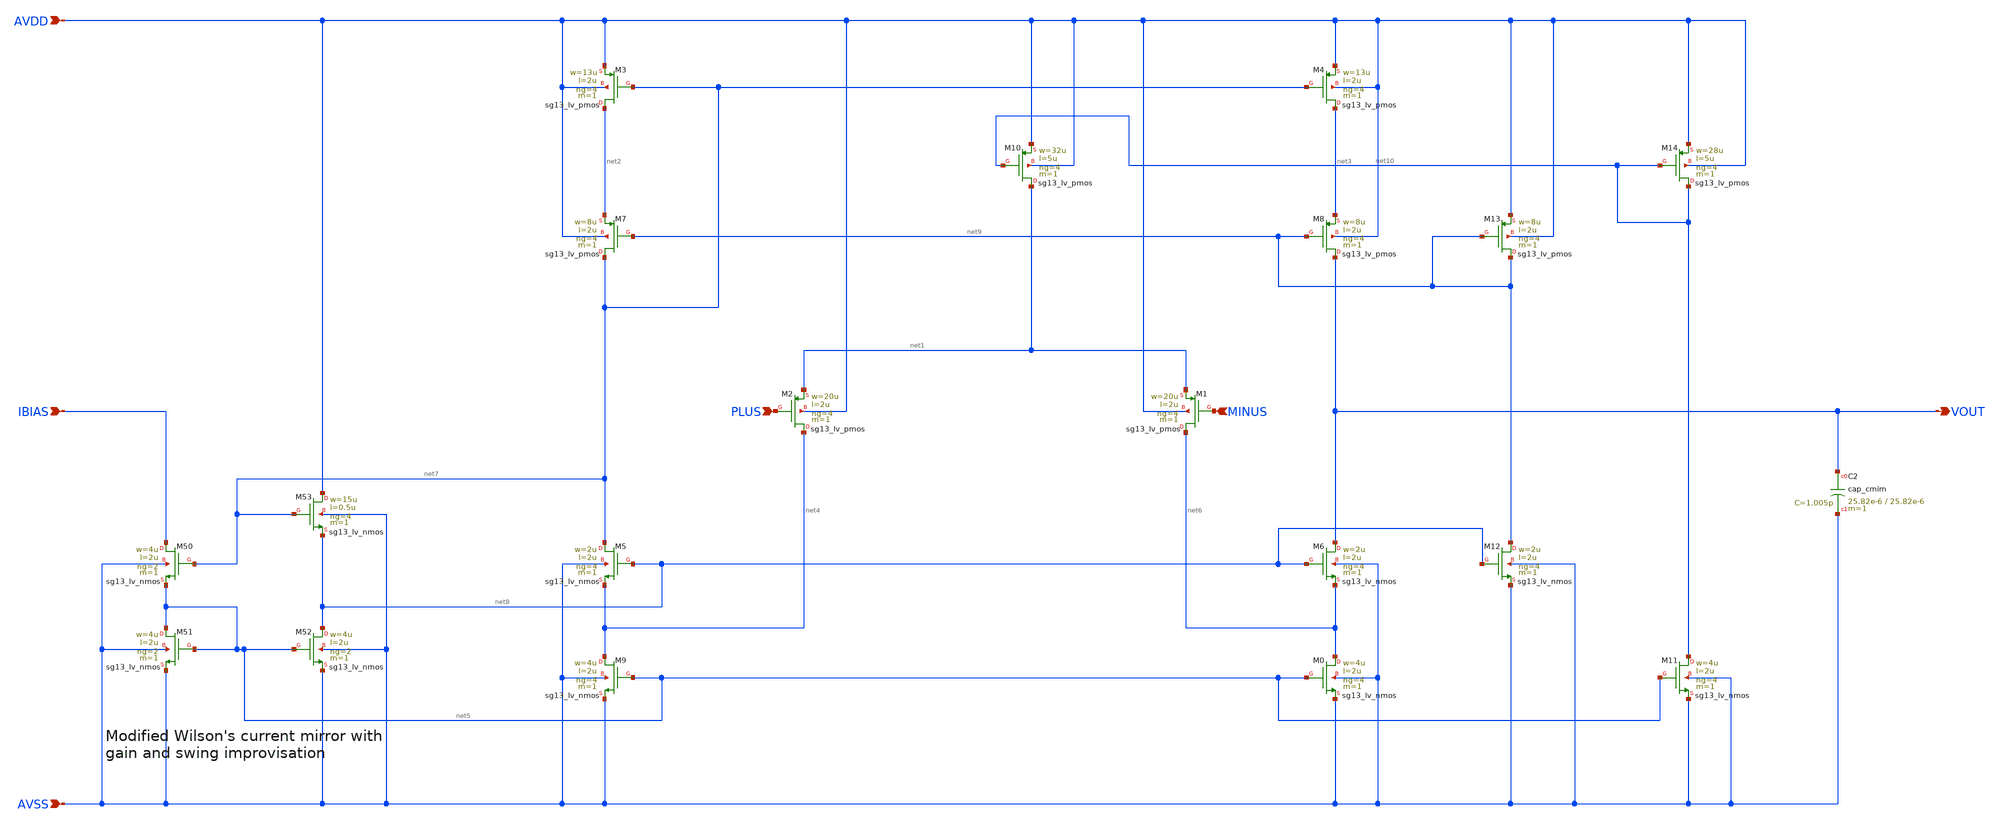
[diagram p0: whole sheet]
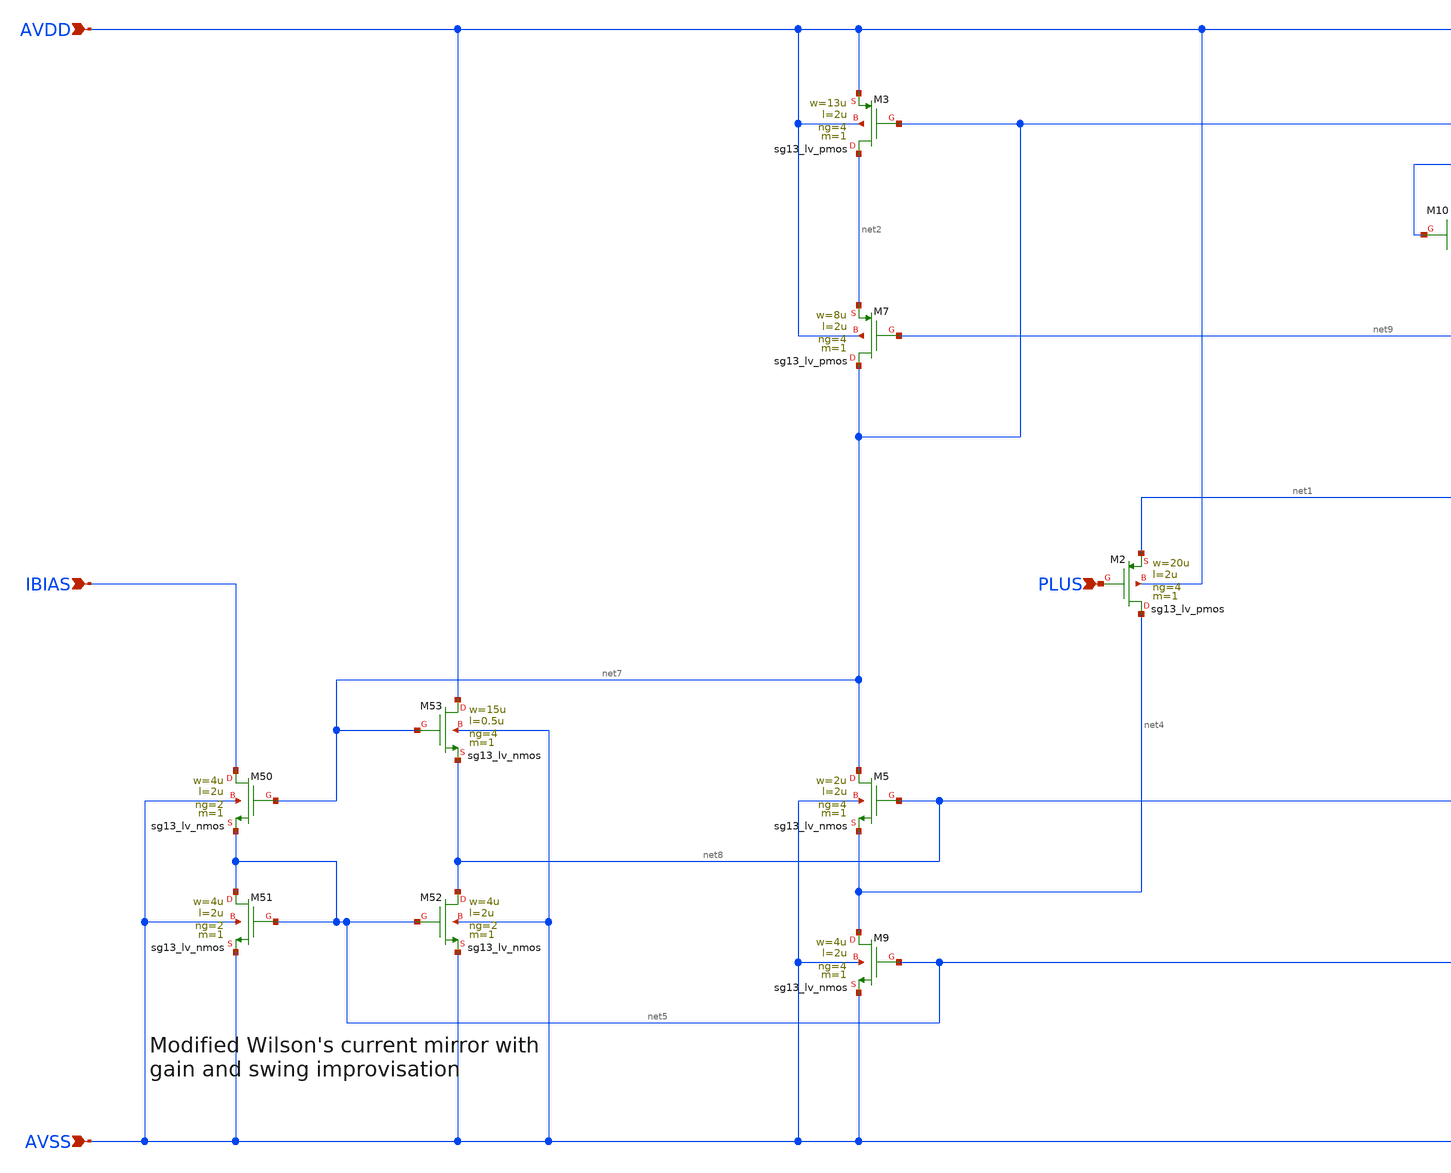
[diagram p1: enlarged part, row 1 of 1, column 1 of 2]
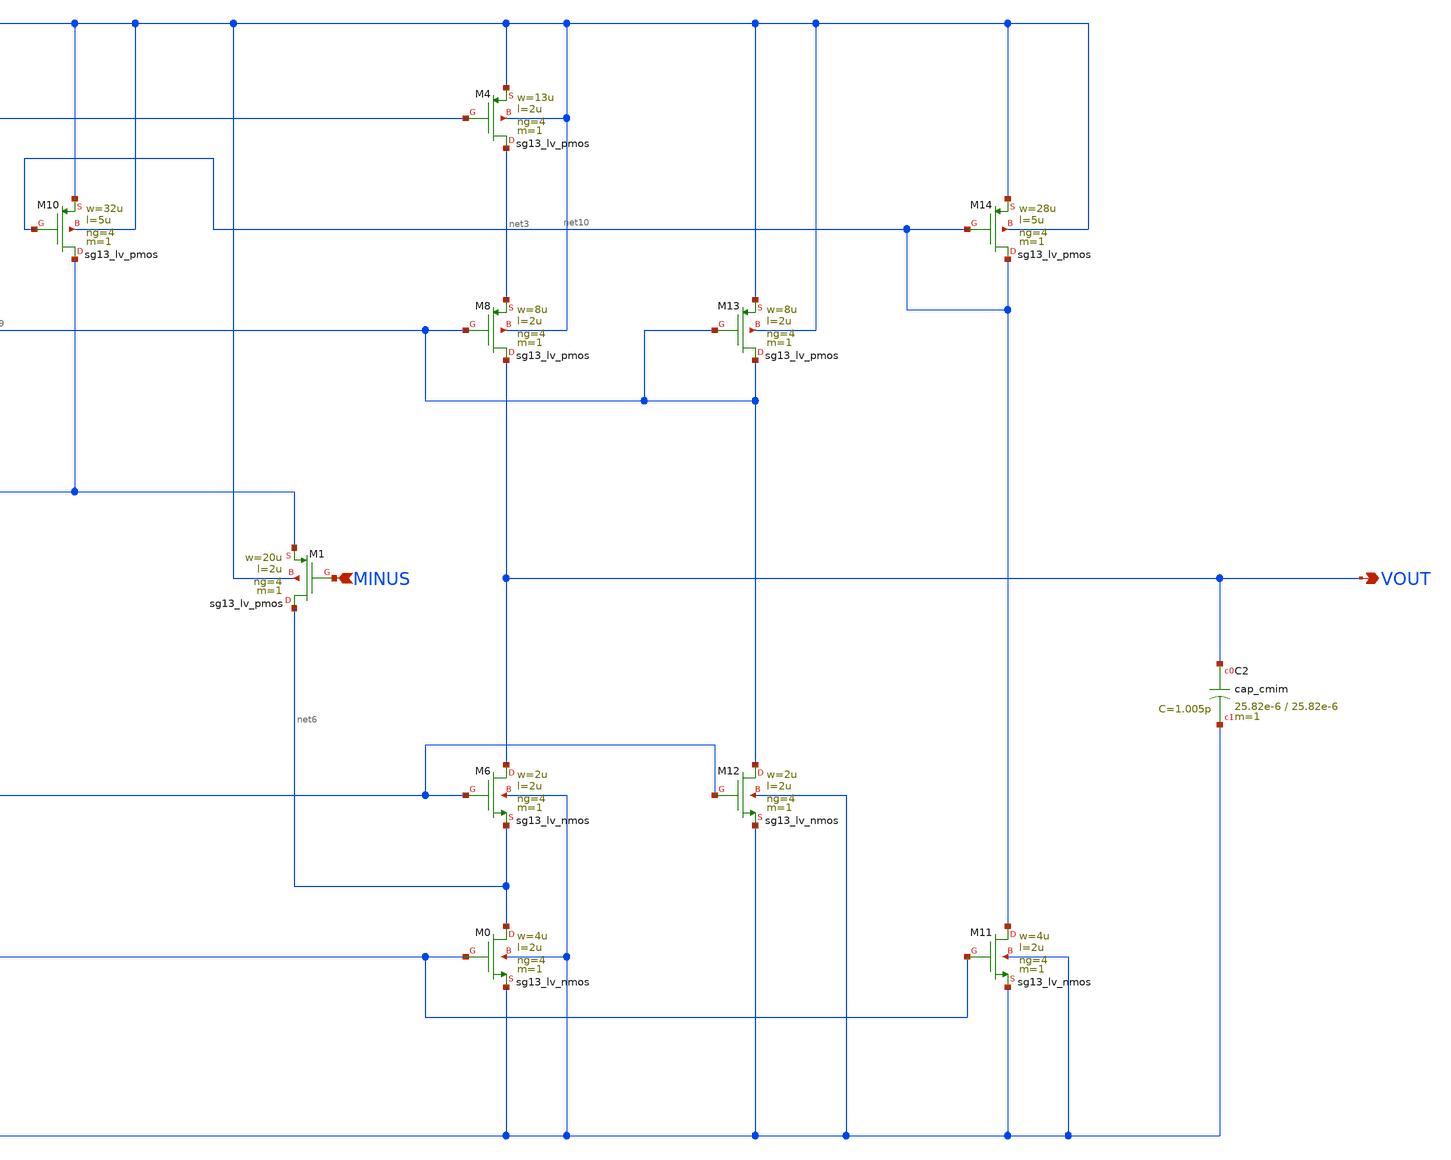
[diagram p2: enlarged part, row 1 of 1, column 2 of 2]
** sch_path: Designs/otas/1_schematics/foldedcascode_pmos.sch
**.subckt foldedcascode_pmos AVDD AVSS IBIAS PLUS MINUS VOUT
*.ipin AVDD
*.ipin AVSS
*.ipin IBIAS
*.ipin PLUS
*.ipin MINUS
*.opin VOUT
XM1 net6 MINUS net1 AVDD sg13_lv_pmos w=20u l=2u ng=4 m=1 mm_ok=1
XM5 net7 net8 net4 AVSS sg13_lv_nmos w=2u l=2u ng=4 m=1 mm_ok=1
XM2 net4 PLUS net1 AVDD sg13_lv_pmos w=20u l=2u ng=4 m=1 mm_ok=1
XM3 net2 net7 AVDD AVDD sg13_lv_pmos w=13u l=2u ng=4 m=1 mm_ok=1
XM4 net3 net7 AVDD AVDD sg13_lv_pmos w=13u l=2u ng=4 m=1 mm_ok=1
XM7 net7 net9 net2 AVDD sg13_lv_pmos w=8u l=2u ng=4 m=1 mm_ok=1
XM8 VOUT net9 net3 AVDD sg13_lv_pmos w=8u l=2u ng=4 m=1 mm_ok=1
XM6 VOUT net8 net6 AVSS sg13_lv_nmos w=2u l=2u ng=4 m=1 mm_ok=1
XM9 net4 net5 AVSS AVSS sg13_lv_nmos w=4u l=2u ng=4 m=1 mm_ok=1
XM0 net6 net5 AVSS AVSS sg13_lv_nmos w=4u l=2u ng=4 m=1 mm_ok=1
XM10 net1 net10 AVDD AVDD sg13_lv_pmos w=32u l=5u ng=4 m=1 mm_ok=1
XM50 IBIAS net7 net5 AVSS sg13_lv_nmos w=4u l=2u ng=2 m=1 mm_ok=1
XM51 net5 net5 AVSS AVSS sg13_lv_nmos w=4u l=2u ng=2 m=1 mm_ok=1
XM52 net8 net5 AVSS AVSS sg13_lv_nmos w=4u l=2u ng=2 m=1 mm_ok=1
XM53 AVDD net7 net8 AVSS sg13_lv_nmos w=15u l=0.5u ng=4 m=1 mm_ok=1
XM12 net9 net8 AVSS AVSS sg13_lv_nmos w=2u l=2u ng=4 m=1 mm_ok=1
XM13 net9 net9 AVDD AVDD sg13_lv_pmos w=8u l=2u ng=4 m=1 mm_ok=1
XM11 net10 net5 AVSS AVSS sg13_lv_nmos w=4u l=2u ng=4 m=1 mm_ok=1
XM14 net10 net10 AVDD AVDD sg13_lv_pmos w=28u l=5u ng=4 m=1 mm_ok=1
XC2 VOUT AVSS cap_cmim w=25.82e-6 l=25.82e-6 m=1 mm_ok=1
**.ends
.end
